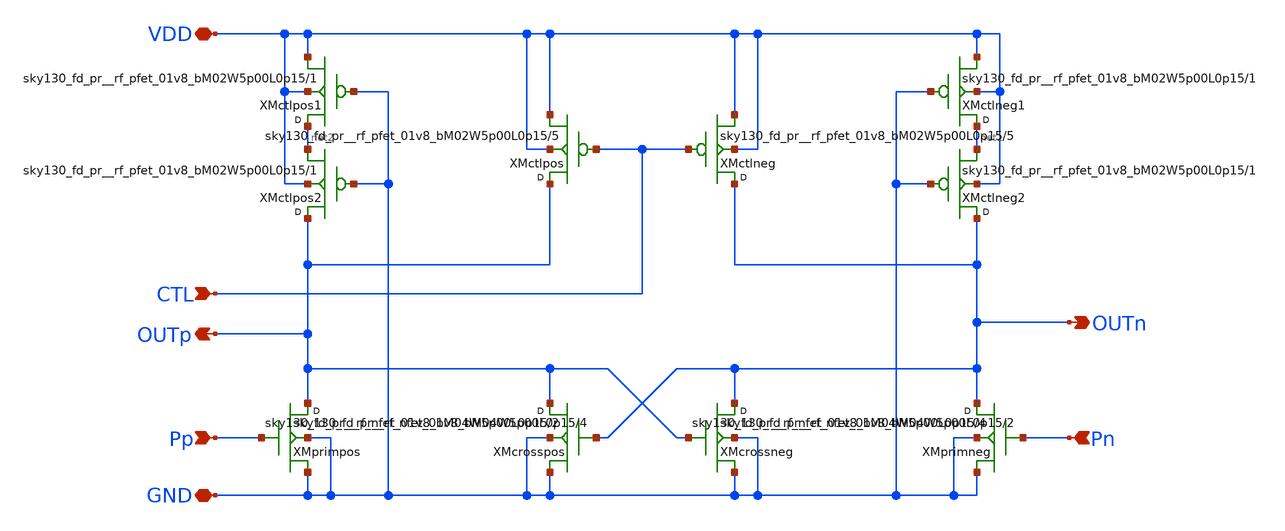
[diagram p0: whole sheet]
** sch_path: design/vco_2-4GHz_delaycell/vco_2-4Ghz_delaycell.sch
**.subckt vco_2-4Ghz_delaycell Pp Pn OUTn OUTp VDD GND CTL
*.ipin Pp
*.ipin Pn
*.opin OUTn
*.opin OUTp
*.iopin VDD
*.iopin GND
*.ipin CTL
XXMprimpos OUTp Pp GND GND sky130_fd_pr__rf_nfet_01v8_bM04W5p00L0p15 m=4
XXMcrossneg OUTn OUTp GND GND sky130_fd_pr__rf_nfet_01v8_bM04W5p00L0p15 m=2
XXMctlneg OUTn CTL VDD VDD sky130_fd_pr__rf_pfet_01v8_bM02W5p00L0p15 m=5
XXMctlpos OUTp CTL VDD VDD sky130_fd_pr__rf_pfet_01v8_bM02W5p00L0p15 m=5
XXMcrosspos OUTp OUTn GND GND sky130_fd_pr__rf_nfet_01v8_bM04W5p00L0p15 m=2
XXMprimneg OUTn Pn GND GND sky130_fd_pr__rf_nfet_01v8_bM04W5p00L0p15 m=4
XXMctlpos1 net2 GND VDD VDD sky130_fd_pr__rf_pfet_01v8_bM02W5p00L0p15 m=1
XXMctlneg1 net1 GND VDD VDD sky130_fd_pr__rf_pfet_01v8_bM02W5p00L0p15 m=1
XXMctlpos2 OUTp GND net2 VDD sky130_fd_pr__rf_pfet_01v8_bM02W5p00L0p15 m=1
XXMctlneg2 OUTn GND net1 VDD sky130_fd_pr__rf_pfet_01v8_bM02W5p00L0p15 m=1
**.ends
.end
